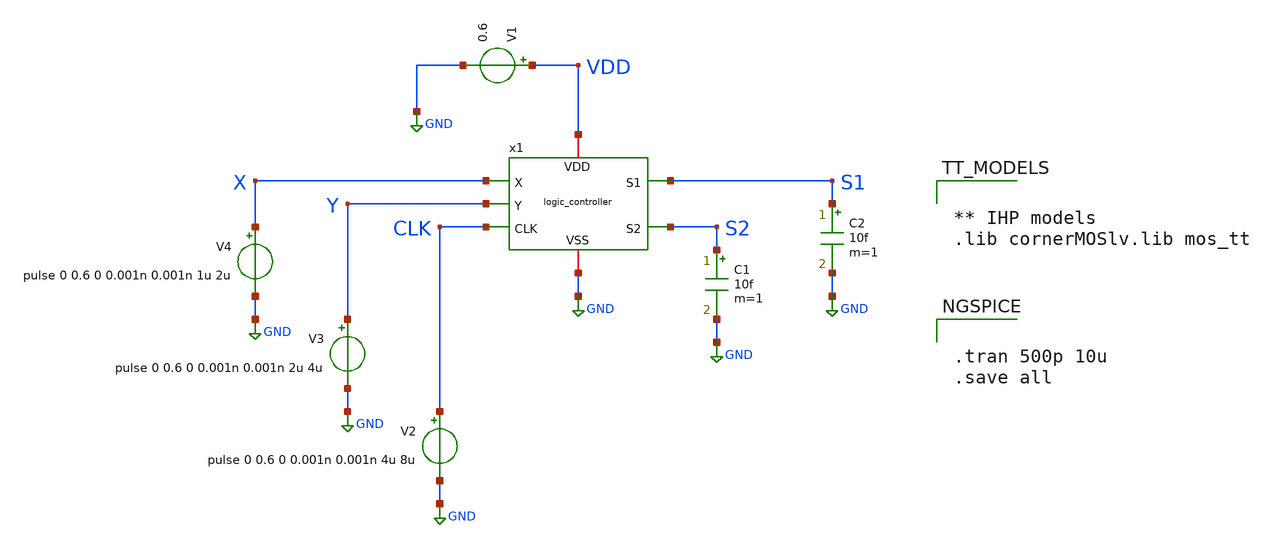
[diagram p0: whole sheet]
** sch_path: SSDOR_1.2V_v3/components/logic_controller/tb_logic_controller.sch
**.subckt tb_logic_controller
x1 VDD X S1 CLK Y S2 GND logic_controller
V1 VDD GND 0.6
C1 S2 GND 10f m=1
C2 S1 GND 10f m=1
V2 CLK GND pulse 0 0.6 0 0.001n 0.001n 4u 8u
V3 Y GND pulse 0 0.6 0 0.001n 0.001n 2u 4u
V4 X GND pulse 0 0.6 0 0.001n 0.001n 1u 2u
**** begin user architecture code


** IHP models
.lib cornerMOSlv.lib mos_tt




.tran 500p 10u
.save all


**** end user architecture code
**.ends
.GLOBAL GND
.end
